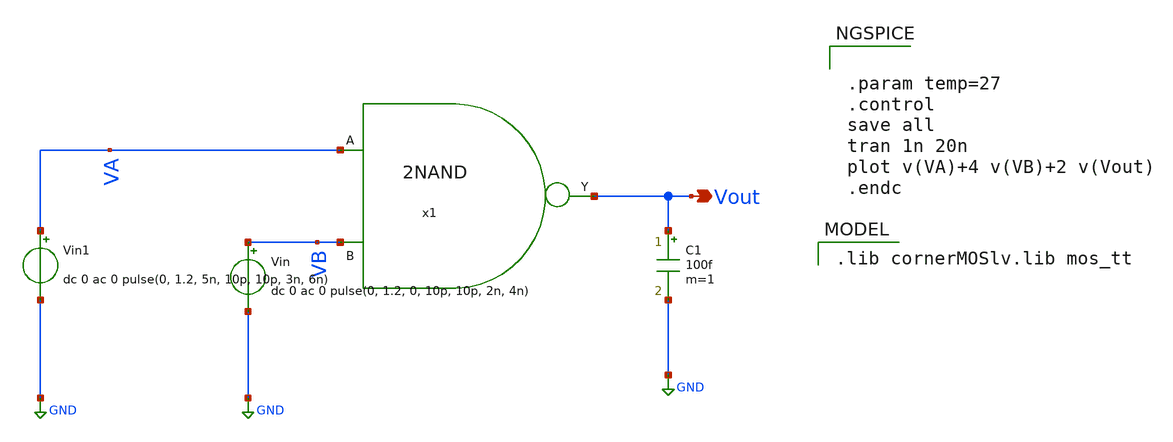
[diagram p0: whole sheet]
** sch_path: Team Designs/Team 1 Design/design_data/xschem/2_Input_NAND/2NAND_tb.sch
**.subckt 2NAND_tb Vout
*.opin Vout
Vin VB GND dc 0 ac 0 pulse(0, 1.2, 0, 10p, 10p, 2n, 4n)
Vin1 VA GND dc 0 ac 0 pulse(0, 1.2, 5n, 10p, 10p, 3n, 6n)
C1 Vout GND 100f m=1
x1 VA Vout VB 2NAND
**** begin user architecture code
 .lib cornerMOSlv.lib mos_tt



.param temp=27
.control
save all
tran 1n 20n
plot v(VA)+4 v(VB)+2 v(Vout)
.endc


**** end user architecture code
**.ends

* expanding   symbol:  /foss/designs/Team1/2NAND/2NAND.sym # of pins=3
** sym_path: Team 1 Design/design_data/xschem/2_Input_NAND/2NAND.sym
** sch_path: Team 1 Design/design_data/xschem/2_Input_NAND/2NAND.sch
.subckt 2NAND A Y B
*.ipin B
*.opin Y
*.ipin A
XM1 Y A net1 net1 sg13_lv_pmos w=2u l=0.13u ng=1 m=1 mm_ok=1
XM2 Y B net1 net1 sg13_lv_pmos w=2u l=0.13u ng=1 m=1 mm_ok=1
XM3 Y B net2 GND sg13_lv_nmos w=1u l=0.13u ng=1 m=1 mm_ok=1
XM4 net2 A GND GND sg13_lv_nmos w=1u l=0.13u ng=1 m=1 mm_ok=1
V1 net1 GND 1.2
.ends

.GLOBAL GND
.end
